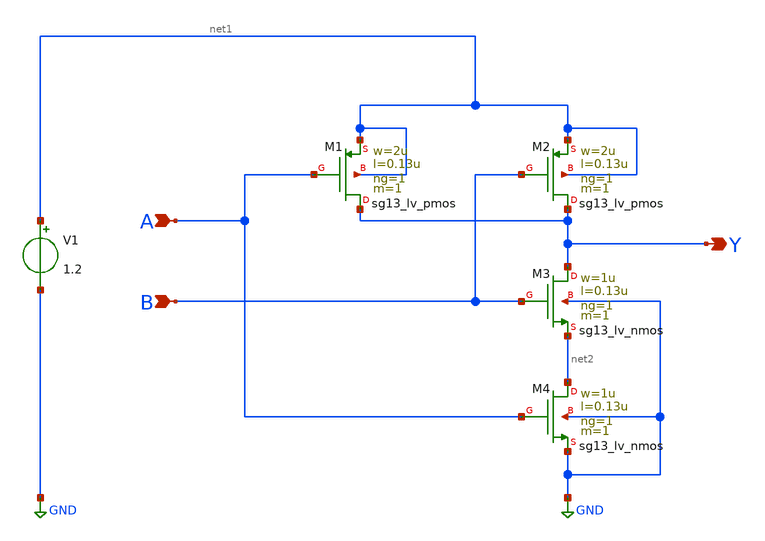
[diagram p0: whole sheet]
** sch_path: Team 1 Design/design_data/xschem/2_Input_NAND/2NAND.sch
**.subckt 2NAND B Y A
*.ipin B
*.opin Y
*.ipin A
XM1 Y A net1 net1 sg13_lv_pmos w=2u l=0.13u ng=1 m=1 mm_ok=1
XM2 Y B net1 net1 sg13_lv_pmos w=2u l=0.13u ng=1 m=1 mm_ok=1
XM3 Y B net2 GND sg13_lv_nmos w=1u l=0.13u ng=1 m=1 mm_ok=1
XM4 net2 A GND GND sg13_lv_nmos w=1u l=0.13u ng=1 m=1 mm_ok=1
V1 net1 GND 1.2
**.ends
.GLOBAL GND
.end
